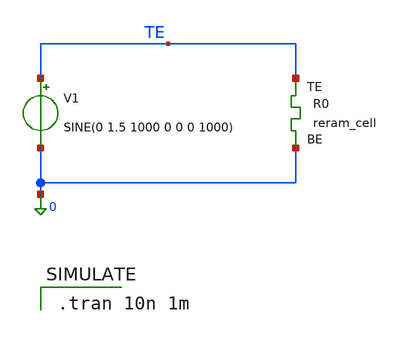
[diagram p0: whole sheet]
** sch_path: Synapse/reram_example_ngspice.sch
**.subckt reram_example_ngspice
V1 TE 0 SINE(0 1.5 1000 0 0 0 1000)
XR0 TE 0 sky130_fd_pr_reram__reram_cell Tfilament_0=3.8e-9
**** begin user architecture code

.tran 10n 1m


** opencircuitdesign pdks install
.inc $::SKYWATER_MODELS/sky130_fd_pr_reram__reram_cell.spice


.control
save all
run
write reram_example_ngspice.raw
.endc



**** end user architecture code
**.ends
.end
